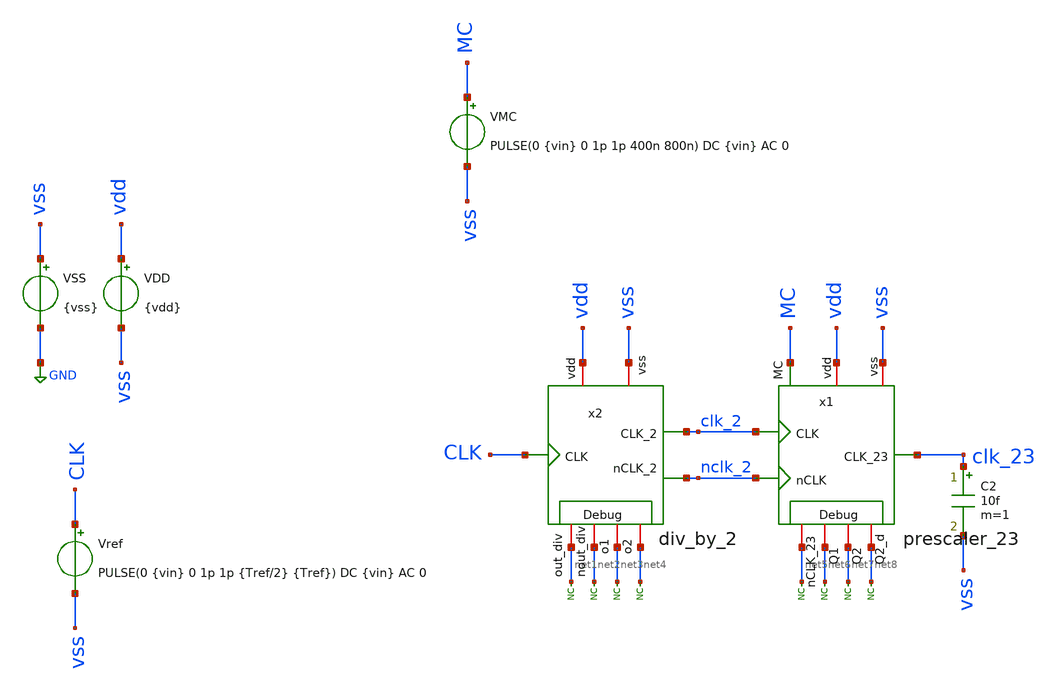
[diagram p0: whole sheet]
** sch_path: xschem/tb_prescaler_23.sch
**.subckt tb_prescaler_23
VSS vss GND {vss}
VDD vdd vss {vdd}
Vref CLK vss PULSE(0 {vin} 0 1p 1p {Tref/2} {Tref}) DC {vin} AC 0
C2 clk_23 vss 10f m=1
x2 nclk_2 vss CLK vdd clk_2 net1 net2 net3 net4 div_by_2
x1 vdd clk_23 clk_2 nclk_2 vss MC net6 net5 net7 net8 prescaler_23
VMC MC vss PULSE(0 {vin} 0 1p 1p 400n 800n) DC {vin} AC 0
* noconn #net1
* noconn #net2
* noconn #net3
* noconn #net4
* noconn #net5
* noconn #net6
* noconn #net7
* noconn #net8
**** begin user architecture code



* Parameters
.param kp = 1.0
.param vdd = kp*1.8
.param vss = 0.0
.param vin = vdd
.param fref = 1e9
.param Tref = 1/fref
.param C = 1f
.param iref=100u

.options TEMP = 100.0
.options RSHUNT = 1e20

* Models
.lib ~/skywater/skywater-pdk/libraries/sky130_fd_pr_ngspice/latest/models/corners/sky130.lib SS

* Data to save
.save all
.ic v(CLK) = 0.0
.ic v(MC) = 0.0
.ic v(clk_2) = 0.0
.ic v(nclk_2) = 0.0
.ic v(clk_23) = 0.0

* Simulation
.control
	tran 0.01ns 800ns
	write tb_div_by_5_tran.raw
	plot v(clk_23) v(clk) v(clk_2) v(clk_23)+3 v(clk_2)+6 v(clk)+9

.endc

.end


**** end user architecture code
**.ends
.GLOBAL GND
**** begin user architecture code
[sky130_models]
**** end user architecture code
.end
